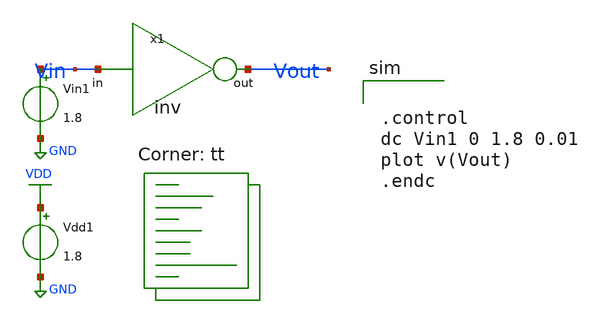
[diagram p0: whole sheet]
** sch_path: tutorial_4/invtest.sch
**.subckt invtest
x1 Vout Vin inv
Vin1 Vin GND 1.8
Vdd1 VDD GND 1.8
**** begin user architecture code


.control
dc Vin1 0 1.8 0.01
plot v(Vout)
.endc

.lib $::SKYWATER_MODELS/sky130.lib.spice tt
**** end user architecture code
**.ends

* expanding   symbol:  /home/EE23B038/ee5311/tutorial_4/inv.sym # of pins=2
** sym_path: tutorial_4/inv.sym
** sch_path: tutorial_4/inv.sch
.subckt inv out in
*.ipin in
*.opin out
XM1 out in GND GND sky130_fd_pr__nfet_01v8 L=0.15 W=0.42 nf=1 ad='int((nf+1)/2) * W/nf * 0.29' as='int((nf+2)/2) * W/nf * 0.29'
+ pd='2*int((nf+1)/2) * (W/nf + 0.29)' ps='2*int((nf+2)/2) * (W/nf + 0.29)' nrd='0.29 / W' nrs='0.29 / W'
+ sa=0 sb=0 sd=0 mult=1 m=1
XM2 out in VDD VDD sky130_fd_pr__pfet_01v8 L=0.15 W={width_p} nf=1 ad='int((nf+1)/2) * W/nf * 0.29' as='int((nf+2)/2) * W/nf * 0.29'
+ pd='2*int((nf+1)/2) * (W/nf + 0.29)' ps='2*int((nf+2)/2) * (W/nf + 0.29)' nrd='0.29 / W' nrs='0.29 / W'
+ sa=0 sb=0 sd=0 mult=1 m=1
.ends

.GLOBAL GND
.GLOBAL VDD
.end
